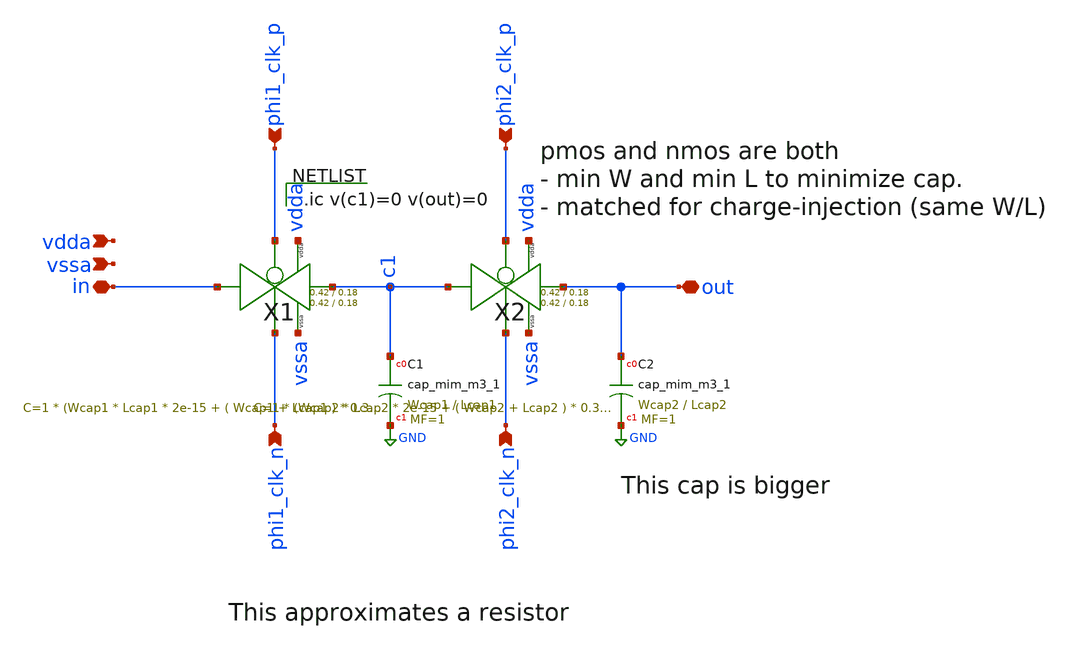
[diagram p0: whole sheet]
** sch_path: xschem/Switched_Caps/2switchcaps.sch
**.subckt 2switchcaps out in phi1_clk_n phi1_clk_p phi2_clk_p phi2_clk_n vdda vssa
*.iopin out
*.iopin in
*.ipin phi1_clk_n
*.ipin phi1_clk_p
*.ipin phi2_clk_p
*.ipin phi2_clk_n
*.ipin vdda
*.ipin vssa
XC1 c1 GND sky130_fd_pr__cap_mim_m3_1 W=Wcap1 L=Lcap1 MF=1 m=1
XC2 out GND sky130_fd_pr__cap_mim_m3_1 W=Wcap2 L=Lcap2 MF=1 m=1
X1 in c1 phi1_clk_p phi1_clk_n vdda vssa transmission_gate Wpmos=0.42 Lpmos=0.18 Wnmos=0.42
+ Lnmos=0.18
X2 c1 out phi2_clk_p phi2_clk_n vdda vssa transmission_gate Wpmos=0.42 Lpmos=0.18 Wnmos=0.42
+ Lnmos=0.18
**** begin user architecture code

.ic v(c1)=0 v(out)=0

**** end user architecture code
**.ends

* expanding   symbol:  transmission_gate/transmission_gate.sym # of pins=6
** sym_path: xschem/transmission_gate/transmission_gate.sym
** sch_path: xschem/transmission_gate/transmission_gate.sch
.subckt transmission_gate in out ctrl_ ctrl vdda vssa  Wpmos=Wpmos Lpmos=Lpmos Wnmos=Wnmos
+ Lnmos=Lnmos
*.iopin in
*.iopin out
*.ipin ctrl_
*.ipin ctrl
*.ipin vdda
*.ipin vssa
XM1 out ctrl in vssa sky130_fd_pr__nfet_01v8 L=Lnmos W=Wnmos nf=1 ad='int((nf+1)/2) * W/nf * 0.29' as='int((nf+2)/2) * W/nf * 0.29'
+ pd='2*int((nf+1)/2) * (W/nf + 0.29)' ps='2*int((nf+2)/2) * (W/nf + 0.29)' nrd='0.29 / W' nrs='0.29 / W'
+ sa=0 sb=0 sd=0 mult=1 m=1
XM2 out ctrl_ in vdda sky130_fd_pr__pfet_01v8 L=Lpmos W=1.26 nf=1 ad='int((nf+1)/2) * W/nf * 0.29' as='int((nf+2)/2) * W/nf * 0.29'
+ pd='2*int((nf+1)/2) * (W/nf + 0.29)' ps='2*int((nf+2)/2) * (W/nf + 0.29)' nrd='0.29 / W' nrs='0.29 / W'
+ sa=0 sb=0 sd=0 mult=1 m=1
.ends

.GLOBAL GND
.end
